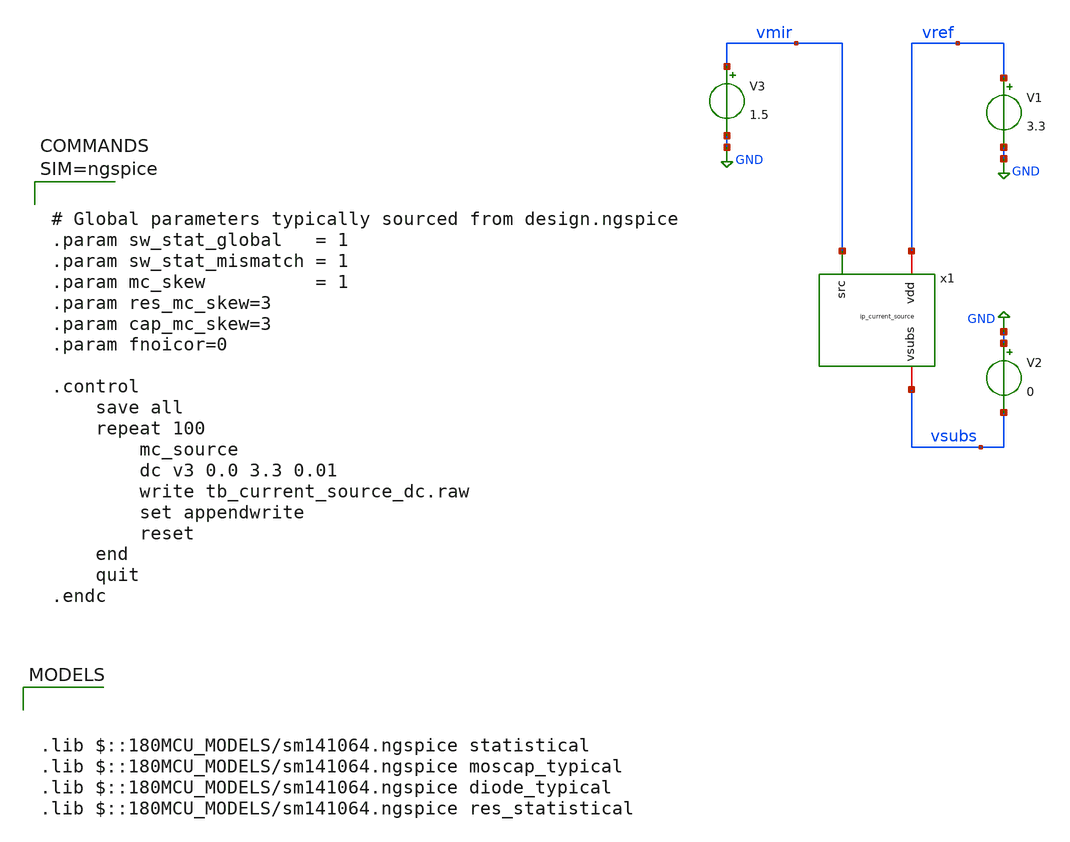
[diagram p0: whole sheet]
** sch_path: xschem/tb_current_source_dc.sch
**.subckt tb_current_source_dc
x1 vref vmir vsubs ip_current_source
V1 vref GND 3.3
V2 GND vsubs 0
V3 vmir GND 1.5
**** begin user architecture code


.lib $::180MCU_MODELS/sm141064.ngspice statistical
.lib $::180MCU_MODELS/sm141064.ngspice moscap_typical
.lib $::180MCU_MODELS/sm141064.ngspice diode_typical
.lib $::180MCU_MODELS/sm141064.ngspice res_statistical




# Global parameters typically sourced from design.ngspice
.param sw_stat_global   = 1
.param sw_stat_mismatch = 1
.param mc_skew          = 1
.param res_mc_skew=3
.param cap_mc_skew=3
.param fnoicor=0

.control
	save all
	repeat 100
		mc_source
		dc v3 0.0 3.3 0.01
		write tb_current_source_dc.raw
		set appendwrite
		reset
	end
	quit
.endc



**** end user architecture code
**.ends

* expanding   symbol:  ip_current_source.sym # of pins=3
** sym_path: xschem/ip_current_source.sym
** sch_path: xschem/ip_current_source.sch
.subckt ip_current_source vdd src vsubs
*.iopin vdd
*.iopin vsubs
*.ipin src
XM1 refin refin vsubs vsubs nfet_03v3 L=1u W=5u nf=1 ad='int((nf+1)/2) * W/nf * 0.18u' as='int((nf+2)/2) * W/nf * 0.18u'
+ pd='2*int((nf+1)/2) * (W/nf + 0.18u)' ps='2*int((nf+2)/2) * (W/nf + 0.18u)' nrd='0.18u / W' nrs='0.18u / W'
+ sa=0 sb=0 sd=0 m=1
XM2 net1 refin vsubs vsubs nfet_03v3 L=5u W=0.5u nf=1 ad='int((nf+1)/2) * W/nf * 0.18u' as='int((nf+2)/2) * W/nf * 0.18u'
+ pd='2*int((nf+1)/2) * (W/nf + 0.18u)' ps='2*int((nf+2)/2) * (W/nf + 0.18u)' nrd='0.18u / W' nrs='0.18u / W'
+ sa=0 sb=0 sd=0 m=1
XM3 src refin net1 vsubs nfet_03v3 L=0.5u W=5u nf=1 ad='int((nf+1)/2) * W/nf * 0.18u' as='int((nf+2)/2) * W/nf * 0.18u'
+ pd='2*int((nf+1)/2) * (W/nf + 0.18u)' ps='2*int((nf+2)/2) * (W/nf + 0.18u)' nrd='0.18u / W' nrs='0.18u / W'
+ sa=0 sb=0 sd=0 m=1
XR1 refin net3 vsubs ppolyf_u_1k r_width=1e-6 r_length=6e-6 m=1
XR2 net3 net2 vsubs ppolyf_u_1k r_width=1e-6 r_length=6e-6 m=1
XR3 net2 net4 vsubs ppolyf_u_1k r_width=1e-6 r_length=6e-6 m=1
XR4 net4 net6 vsubs ppolyf_u_1k r_width=1e-6 r_length=6e-6 m=1
XR5 net6 net5 vsubs ppolyf_u_1k r_width=1e-6 r_length=6e-6 m=1
XR6 net5 vdd vsubs ppolyf_u_1k r_width=1e-6 r_length=6e-6 m=1
XM4 src refin net1 vsubs nfet_03v3 L=0.5u W=5u nf=1 ad='int((nf+1)/2) * W/nf * 0.18u' as='int((nf+2)/2) * W/nf * 0.18u'
+ pd='2*int((nf+1)/2) * (W/nf + 0.18u)' ps='2*int((nf+2)/2) * (W/nf + 0.18u)' nrd='0.18u / W' nrs='0.18u / W'
+ sa=0 sb=0 sd=0 m=1
.ends

.GLOBAL GND
.end
